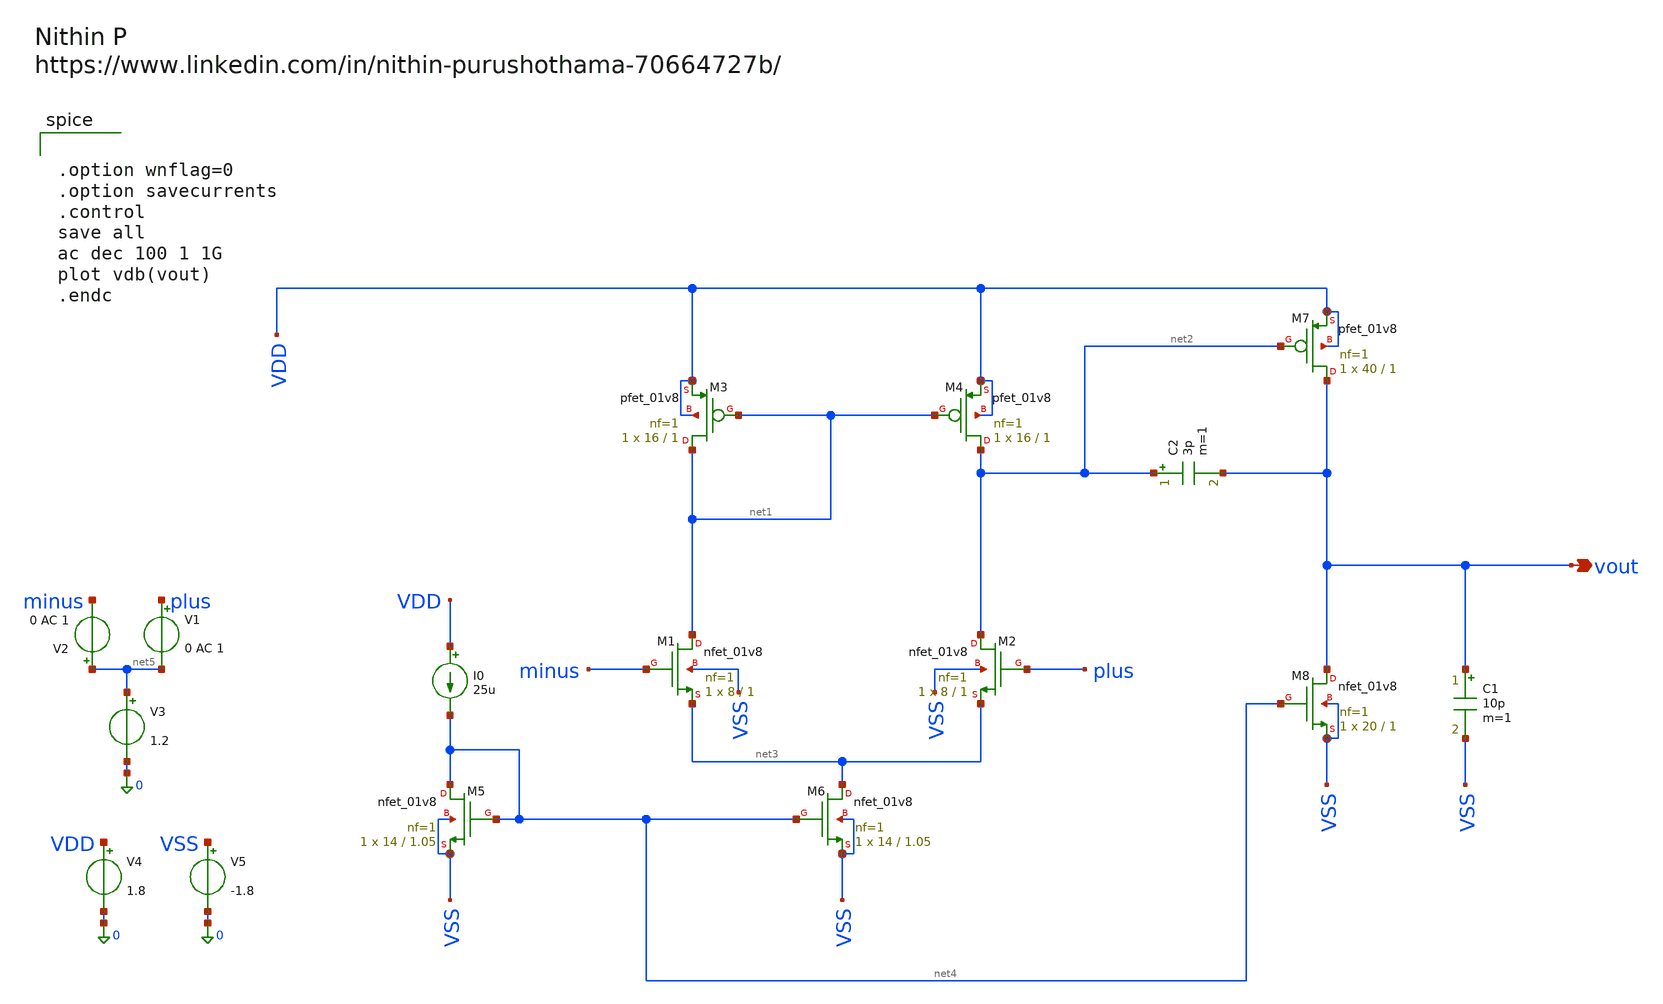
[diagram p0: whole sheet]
** sch_path: 2stageopamppt3.sch
**.subckt 2stageopamppt3 vout
*.opin vout
C2 net2 vout 3p m=1
C1 vout VSS 10p m=1
I0 VDD net4 25u
V1 plus net5 0 AC 1
V2 net5 minus 0 AC 1
V3 net5 0 1.2
V4 VDD 0 1.8
V5 VSS 0 -1.8
XM1 net1 minus net3 VSS sky130_fd_pr__nfet_01v8 L=1 W=8 nf=1 ad='int((1 + 1)/2) * 8 / 1 * 0.29' as='int((1 + 2)/2) * 8 / 1 * 0.29'
+ pd='2*int((1 + 1)/2) * (8 / 1 + 0.29)' ps='2*int((1 + 2)/2) * (8 / 1 + 0.29)' nrd='0.29 / 8 ' nrs='0.29 / 8 '
+ sa=0 sb=0 sd=0 mult=1 m=1
XM2 net2 plus net3 VSS sky130_fd_pr__nfet_01v8 L=1 W=8 nf=1 ad='int((1 + 1)/2) * 8 / 1 * 0.29' as='int((1 + 2)/2) * 8 / 1 * 0.29'
+ pd='2*int((1 + 1)/2) * (8 / 1 + 0.29)' ps='2*int((1 + 2)/2) * (8 / 1 + 0.29)' nrd='0.29 / 8 ' nrs='0.29 / 8 '
+ sa=0 sb=0 sd=0 mult=1 m=1
XM3 net1 net1 VDD VDD sky130_fd_pr__pfet_01v8 L=1 W=16 nf=1 ad='int((1 + 1)/2) * 16 / 1 * 0.29' as='int((1 + 2)/2) * 16 / 1 * 0.29'
+ pd='2*int((1 + 1)/2) * (16 / 1 + 0.29)' ps='2*int((1 + 2)/2) * (16 / 1 + 0.29)' nrd='0.29 / 16 ' nrs='0.29 / 16 '
+ sa=0 sb=0 sd=0 mult=1 m=1
XM4 net2 net1 VDD VDD sky130_fd_pr__pfet_01v8 L=1 W=16 nf=1 ad='int((1 + 1)/2) * 16 / 1 * 0.29' as='int((1 + 2)/2) * 16 / 1 * 0.29'
+ pd='2*int((1 + 1)/2) * (16 / 1 + 0.29)' ps='2*int((1 + 2)/2) * (16 / 1 + 0.29)' nrd='0.29 / 16 ' nrs='0.29 / 16 '
+ sa=0 sb=0 sd=0 mult=1 m=1
XM5 net4 net4 VSS VSS sky130_fd_pr__nfet_01v8 L=1.05 W=14 nf=1 ad='int((1 + 1)/2) * 14 / 1 * 0.29' as='int((1 + 2)/2) * 14 / 1 * 0.29'
+ pd='2*int((1 + 1)/2) * (14 / 1 + 0.29)' ps='2*int((1 + 2)/2) * (14 / 1 + 0.29)' nrd='0.29 / 14 ' nrs='0.29 / 14 '
+ sa=0 sb=0 sd=0 mult=1 m=1
XM6 net3 net4 VSS VSS sky130_fd_pr__nfet_01v8 L=1.05 W=14 nf=1 ad='int((1 + 1)/2) * 14 / 1 * 0.29' as='int((1 + 2)/2) * 14 / 1 * 0.29'
+ pd='2*int((1 + 1)/2) * (14 / 1 + 0.29)' ps='2*int((1 + 2)/2) * (14 / 1 + 0.29)' nrd='0.29 / 14 ' nrs='0.29 / 14 '
+ sa=0 sb=0 sd=0 mult=1 m=1
XM7 vout net2 VDD VDD sky130_fd_pr__pfet_01v8 L=1 W=40 nf=1 ad='int((1 + 1)/2) * 40 / 1 * 0.29' as='int((1 + 2)/2) * 40 / 1 * 0.29'
+ pd='2*int((1 + 1)/2) * (40 / 1 + 0.29)' ps='2*int((1 + 2)/2) * (40 / 1 + 0.29)' nrd='0.29 / 40 ' nrs='0.29 / 40 '
+ sa=0 sb=0 sd=0 mult=1 m=1
XM8 vout net4 VSS VSS sky130_fd_pr__nfet_01v8 L=1 W=20 nf=1 ad='int((1 + 1)/2) * 20 / 1 * 0.29' as='int((1 + 2)/2) * 20 / 1 * 0.29'
+ pd='2*int((1 + 1)/2) * (20 / 1 + 0.29)' ps='2*int((1 + 2)/2) * (20 / 1 + 0.29)' nrd='0.29 / 20 ' nrs='0.29 / 20 '
+ sa=0 sb=0 sd=0 mult=1 m=1
**** begin user architecture code


.option wnflag=0
.option savecurrents
.control
save all
ac dec 100 1 1G
plot vdb(vout)
.endc



 .lib /foss/pdks/sky130A/libs.tech/ngspice/sky130.lib.spice tt

.param mc_mm_switch=0
.param mc_pr_switch=1

**** end user architecture code
**.ends
.end
